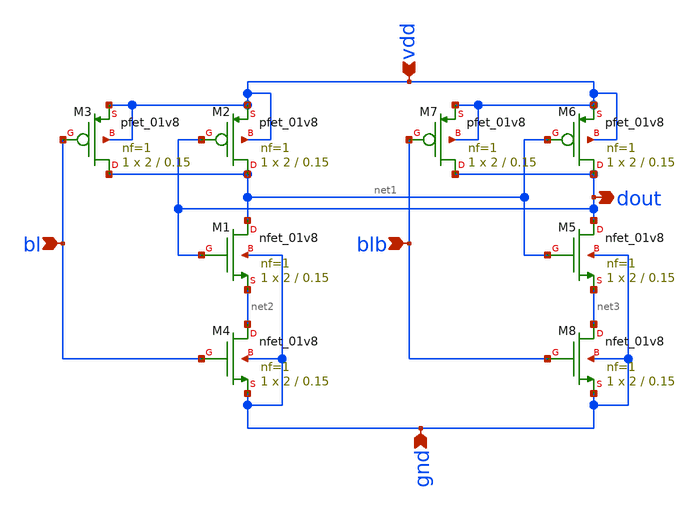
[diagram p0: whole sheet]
** sch_path: Projects/Schematic_Design_and_Analysis_of_an_8-Word_8-Bit_Static_RAM_with_6T_Storage_Cells_using_SKY130PDK/assets/schematic/nand_latch.sch
**.subckt nand_latch vdd dout bl blb gnd
*.ipin vdd
*.opin dout
*.ipin bl
*.ipin blb
*.ipin gnd
XM1 net1 dout net2 gnd sky130_fd_pr__nfet_01v8 L=0.15 W=2 nf=1 ad='int((nf+1)/2) * W/nf * 0.29' as='int((nf+2)/2) * W/nf * 0.29'
+ pd='2*int((nf+1)/2) * (W/nf + 0.29)' ps='2*int((nf+2)/2) * (W/nf + 0.29)' nrd='0.29 / W' nrs='0.29 / W'
+ sa=0 sb=0 sd=0 mult=1 m=1
XM2 net1 dout vdd vdd sky130_fd_pr__pfet_01v8 L=0.15 W=2 nf=1 ad='int((nf+1)/2) * W/nf * 0.29' as='int((nf+2)/2) * W/nf * 0.29'
+ pd='2*int((nf+1)/2) * (W/nf + 0.29)' ps='2*int((nf+2)/2) * (W/nf + 0.29)' nrd='0.29 / W' nrs='0.29 / W'
+ sa=0 sb=0 sd=0 mult=1 m=1
XM3 net1 bl vdd vdd sky130_fd_pr__pfet_01v8 L=0.15 W=2 nf=1 ad='int((nf+1)/2) * W/nf * 0.29' as='int((nf+2)/2) * W/nf * 0.29'
+ pd='2*int((nf+1)/2) * (W/nf + 0.29)' ps='2*int((nf+2)/2) * (W/nf + 0.29)' nrd='0.29 / W' nrs='0.29 / W'
+ sa=0 sb=0 sd=0 mult=1 m=1
XM4 net2 bl gnd gnd sky130_fd_pr__nfet_01v8 L=0.15 W=2 nf=1 ad='int((nf+1)/2) * W/nf * 0.29' as='int((nf+2)/2) * W/nf * 0.29'
+ pd='2*int((nf+1)/2) * (W/nf + 0.29)' ps='2*int((nf+2)/2) * (W/nf + 0.29)' nrd='0.29 / W' nrs='0.29 / W'
+ sa=0 sb=0 sd=0 mult=1 m=1
XM5 dout net1 net3 gnd sky130_fd_pr__nfet_01v8 L=0.15 W=2 nf=1 ad='int((nf+1)/2) * W/nf * 0.29' as='int((nf+2)/2) * W/nf * 0.29'
+ pd='2*int((nf+1)/2) * (W/nf + 0.29)' ps='2*int((nf+2)/2) * (W/nf + 0.29)' nrd='0.29 / W' nrs='0.29 / W'
+ sa=0 sb=0 sd=0 mult=1 m=1
XM6 dout net1 vdd vdd sky130_fd_pr__pfet_01v8 L=0.15 W=2 nf=1 ad='int((nf+1)/2) * W/nf * 0.29' as='int((nf+2)/2) * W/nf * 0.29'
+ pd='2*int((nf+1)/2) * (W/nf + 0.29)' ps='2*int((nf+2)/2) * (W/nf + 0.29)' nrd='0.29 / W' nrs='0.29 / W'
+ sa=0 sb=0 sd=0 mult=1 m=1
XM7 dout blb vdd vdd sky130_fd_pr__pfet_01v8 L=0.15 W=2 nf=1 ad='int((nf+1)/2) * W/nf * 0.29' as='int((nf+2)/2) * W/nf * 0.29'
+ pd='2*int((nf+1)/2) * (W/nf + 0.29)' ps='2*int((nf+2)/2) * (W/nf + 0.29)' nrd='0.29 / W' nrs='0.29 / W'
+ sa=0 sb=0 sd=0 mult=1 m=1
XM8 net3 blb gnd gnd sky130_fd_pr__nfet_01v8 L=0.15 W=2 nf=1 ad='int((nf+1)/2) * W/nf * 0.29' as='int((nf+2)/2) * W/nf * 0.29'
+ pd='2*int((nf+1)/2) * (W/nf + 0.29)' ps='2*int((nf+2)/2) * (W/nf + 0.29)' nrd='0.29 / W' nrs='0.29 / W'
+ sa=0 sb=0 sd=0 mult=1 m=1
**.ends
.end
